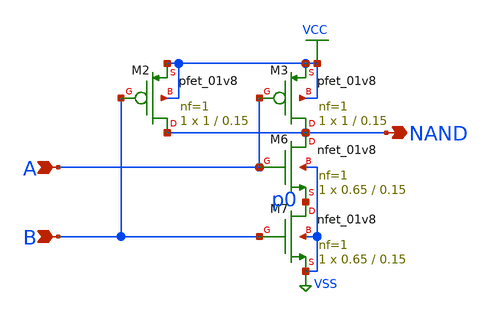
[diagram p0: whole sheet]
** sch_path: blocks/rom/rom_nand2.sch
**.subckt rom_nand2 A NAND B
*.ipin A
*.opin NAND
*.ipin B
XM2 NAND B VCC VCC sky130_fd_pr__pfet_01v8 L=0.15 W=1 nf=1 ad='int((nf+1)/2) * W/nf * 0.29' as='int((nf+2)/2) * W/nf * 0.29'
+ pd='2*int((nf+1)/2) * (W/nf + 0.29)' ps='2*int((nf+2)/2) * (W/nf + 0.29)' nrd='0.29 / W' nrs='0.29 / W'
+ sa=0 sb=0 sd=0 mult=1 m=1
XM3 NAND A VCC VCC sky130_fd_pr__pfet_01v8 L=0.15 W=1 nf=1 ad='int((nf+1)/2) * W/nf * 0.29' as='int((nf+2)/2) * W/nf * 0.29'
+ pd='2*int((nf+1)/2) * (W/nf + 0.29)' ps='2*int((nf+2)/2) * (W/nf + 0.29)' nrd='0.29 / W' nrs='0.29 / W'
+ sa=0 sb=0 sd=0 mult=1 m=1
XM6 NAND A p0 VSS sky130_fd_pr__nfet_01v8 L=0.15 W=0.65 nf=1 ad='int((1 + 1)/2) * 0.65 / 1 * 0.29' as='int((1 + 2)/2) * 0.65 / 1 * 0.29'
+ pd='2*int((1 + 1)/2) * (0.65 / 1 + 0.29)' ps='2*int((1 + 2)/2) * (0.65 / 1 + 0.29)' nrd='0.29 / 0.65 '
+ nrs='0.29 / 0.65 ' sa=0 sb=0 sd=0 mult=1 m=1
XM7 p0 B VSS VSS sky130_fd_pr__nfet_01v8 L=0.15 W=0.65 nf=1 ad='int((1 + 1)/2) * 0.65 / 1 * 0.29' as='int((1 + 2)/2) * 0.65 / 1 * 0.29'
+ pd='2*int((1 + 1)/2) * (0.65 / 1 + 0.29)' ps='2*int((1 + 2)/2) * (0.65 / 1 + 0.29)' nrd='0.29 / 0.65 '
+ nrs='0.29 / 0.65 ' sa=0 sb=0 sd=0 mult=1 m=1
**.ends
.GLOBAL VCC
.GLOBAL VSS
.end
